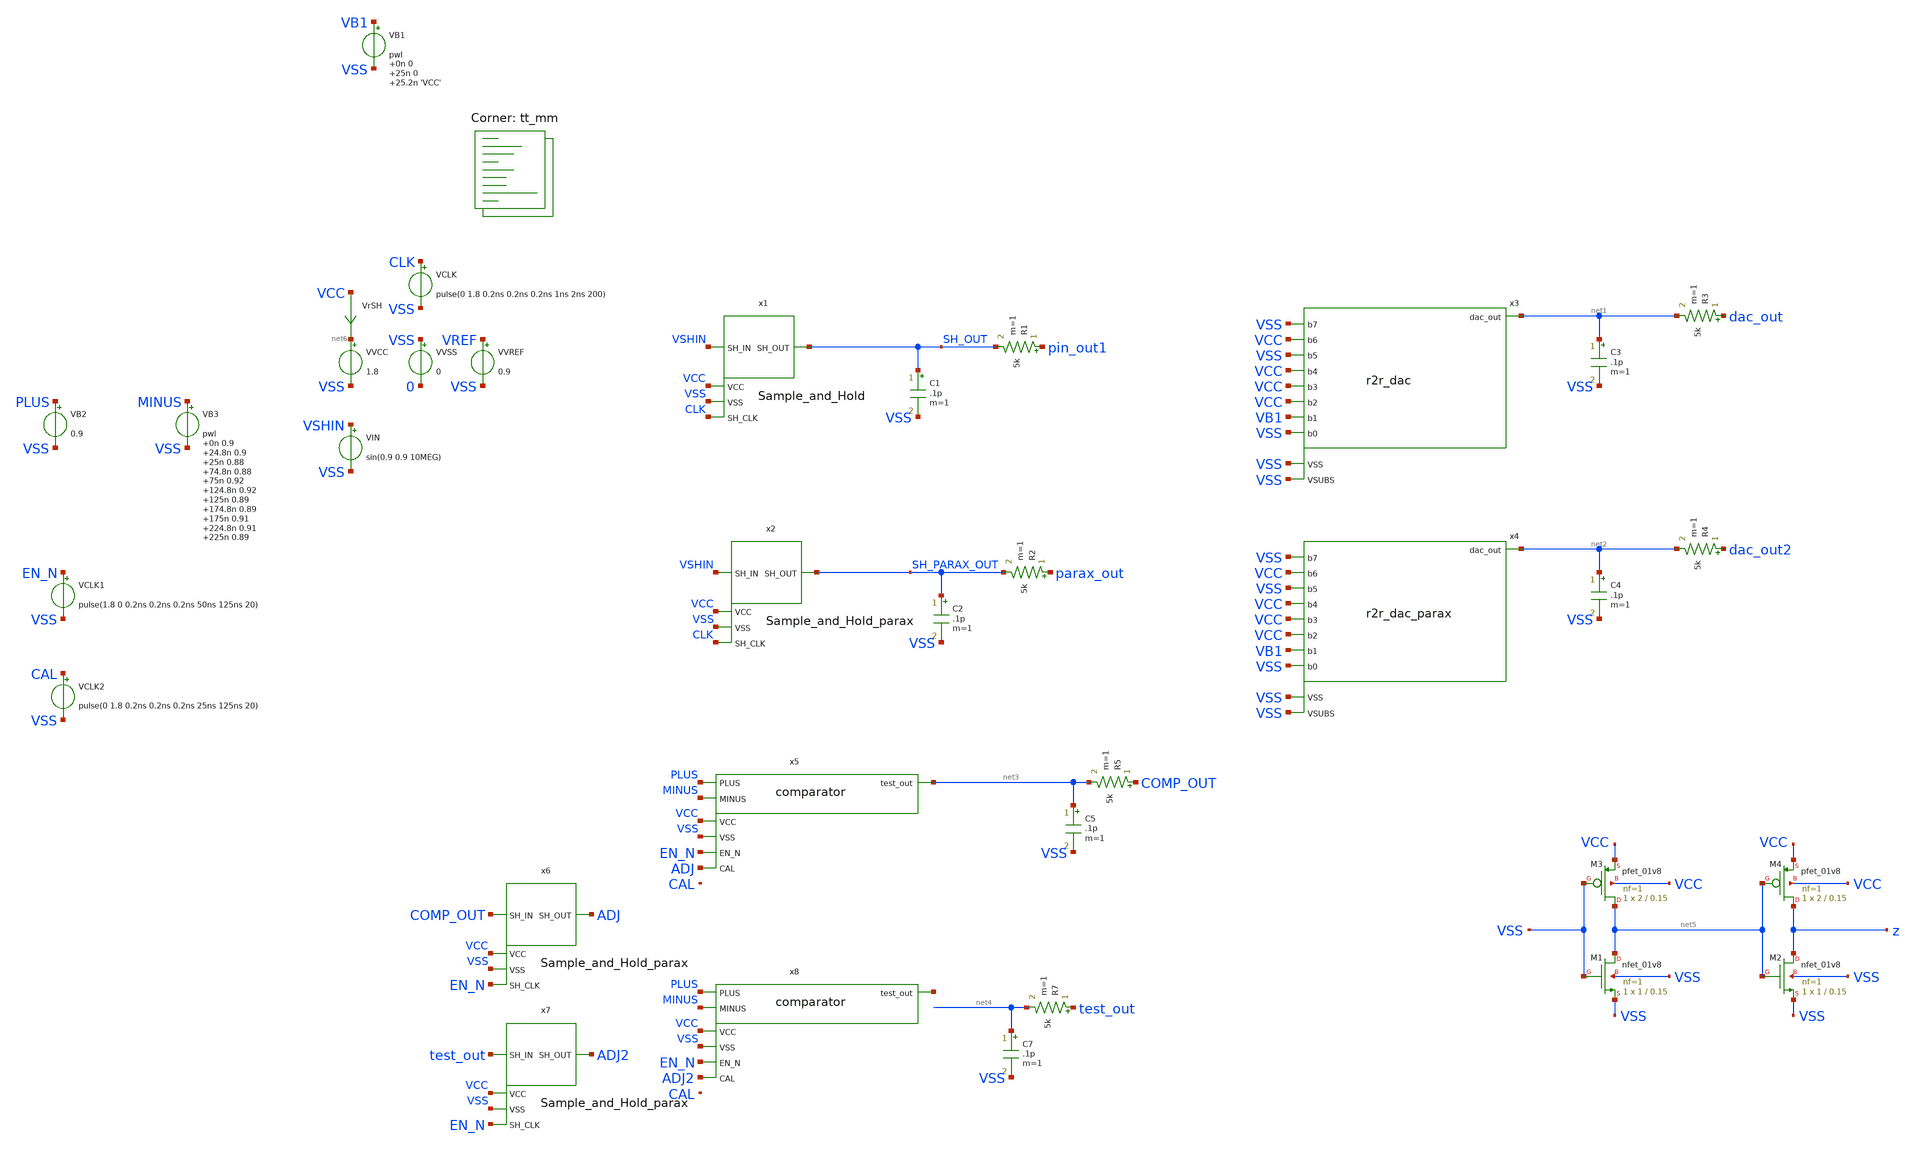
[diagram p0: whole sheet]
** sch_path: xschem/testbench.sch
**.subckt testbench
x1 SH_OUT VSHIN VSS VCC CLK Sample_and_Hold
VCLK CLK VSS pulse(0 1.8 0.2ns 0.2ns 0.2ns 1ns 2ns 200)
VVCC net6 VSS 1.8
VVSS VSS 0 0
VIN VSHIN VSS sin(0.9 0.9 10MEG)
VVREF VREF VSS 0.9
R1 pin_out1 SH_OUT 5k m=1
C1 SH_OUT VSS .1p m=1
VrSH VCC net6 0
.save i(vrsh)
x2 SH_PARAX_OUT VSHIN VSS VCC CLK Sample_and_Hold_parax
R2 parax_out SH_PARAX_OUT 5k m=1
C2 SH_PARAX_OUT VSS .1p m=1
x3 net1 VSS VB1 VCC VCC VSS VSS VCC VCC VSS VSS r2r_dac
VB1 VB1 VSS pwl 0n 0 25n 0 25.2n 'VCC'
R3 dac_out net1 5k m=1
C3 net1 VSS .1p m=1
x4 net2 VSS VB1 VCC VCC VSS VSS VCC VCC VSS VSS r2r_dac_parax
R4 dac_out2 net2 5k m=1
C4 net2 VSS .1p m=1
x5 VCC VSS EN_N PLUS MINUS ADJ net3 comparator
x6 ADJ COMP_OUT VSS VCC EN_N Sample_and_Hold_parax
R5 COMP_OUT net3 5k m=1
C5 net3 VSS .1p m=1
x7 ADJ2 test_out VSS VCC EN_N Sample_and_Hold_parax
R7 test_out net4 5k m=1
C7 net4 VSS .1p m=1
x8 VCC VSS EN_N PLUS MINUS ADJ2 net7 comparator
VB2 PLUS VSS 0.9
VB3 MINUS VSS pwl 0n 0.9 24.8n 0.9 25n 0.88 74.8n 0.88 75n 0.92 124.8n 0.92 125n 0.89 174.8n 0.89
+ 175n 0.91 224.8n 0.91 225n 0.89
VCLK1 EN_N VSS pulse(1.8 0 0.2ns 0.2ns 0.2ns 50ns 125ns 20)
XM1 net5 VSS VSS VSS sky130_fd_pr__nfet_01v8 L=0.15 W=1 nf=1 ad='int((nf+1)/2) * W/nf * 0.29' as='int((nf+2)/2) * W/nf * 0.29'
+ pd='2*int((nf+1)/2) * (W/nf + 0.29)' ps='2*int((nf+2)/2) * (W/nf + 0.29)' nrd='0.29 / W' nrs='0.29 / W'
+ sa=0 sb=0 sd=0 mult=1 m=1
XM2 z net5 VSS VSS sky130_fd_pr__nfet_01v8 L=0.15 W=1 nf=1 ad='int((nf+1)/2) * W/nf * 0.29' as='int((nf+2)/2) * W/nf * 0.29'
+ pd='2*int((nf+1)/2) * (W/nf + 0.29)' ps='2*int((nf+2)/2) * (W/nf + 0.29)' nrd='0.29 / W' nrs='0.29 / W'
+ sa=0 sb=0 sd=0 mult=1 m=1
XM3 net5 VSS VCC VCC sky130_fd_pr__pfet_01v8 L=0.15 W=2 nf=1 ad='int((nf+1)/2) * W/nf * 0.29' as='int((nf+2)/2) * W/nf * 0.29'
+ pd='2*int((nf+1)/2) * (W/nf + 0.29)' ps='2*int((nf+2)/2) * (W/nf + 0.29)' nrd='0.29 / W' nrs='0.29 / W'
+ sa=0 sb=0 sd=0 mult=1 m=1
XM4 z net5 VCC VCC sky130_fd_pr__pfet_01v8 L=0.15 W=2 nf=1 ad='int((nf+1)/2) * W/nf * 0.29' as='int((nf+2)/2) * W/nf * 0.29'
+ pd='2*int((nf+1)/2) * (W/nf + 0.29)' ps='2*int((nf+2)/2) * (W/nf + 0.29)' nrd='0.29 / W' nrs='0.29 / W'
+ sa=0 sb=0 sd=0 mult=1 m=1
VCLK2 CAL VSS pulse(0 1.8 0.2ns 0.2ns 0.2ns 25ns 125ns 20)
**** begin user architecture code
.lib $::SKYWATER_MODELS/sky130.lib.spice tt_mm


.option chgtol=4e-16 method=gear
.param VCC = 1.8
.param VREF = 0.9
.param temp = 25
*vvcc VCC 0 1.8
*vvss VSS 0 0
*vvref VREF 0 0.9
*vclk CLK pulse(1ns 1ns 1ns 5ns 10ns 25)
*vvshin VSHIN sin(0.9 0.9 10MEG)


.control
  save all
  savecurrents
  op
  write testbench.raw
  reset
  set appendwrite
  *repeat 5
    save all
    tran 0.1n 250n uic
    write testbench.raw
    set appendwrite
    reset
  *end
  quit 0
.endc

**** end user architecture code
**.ends
.end
